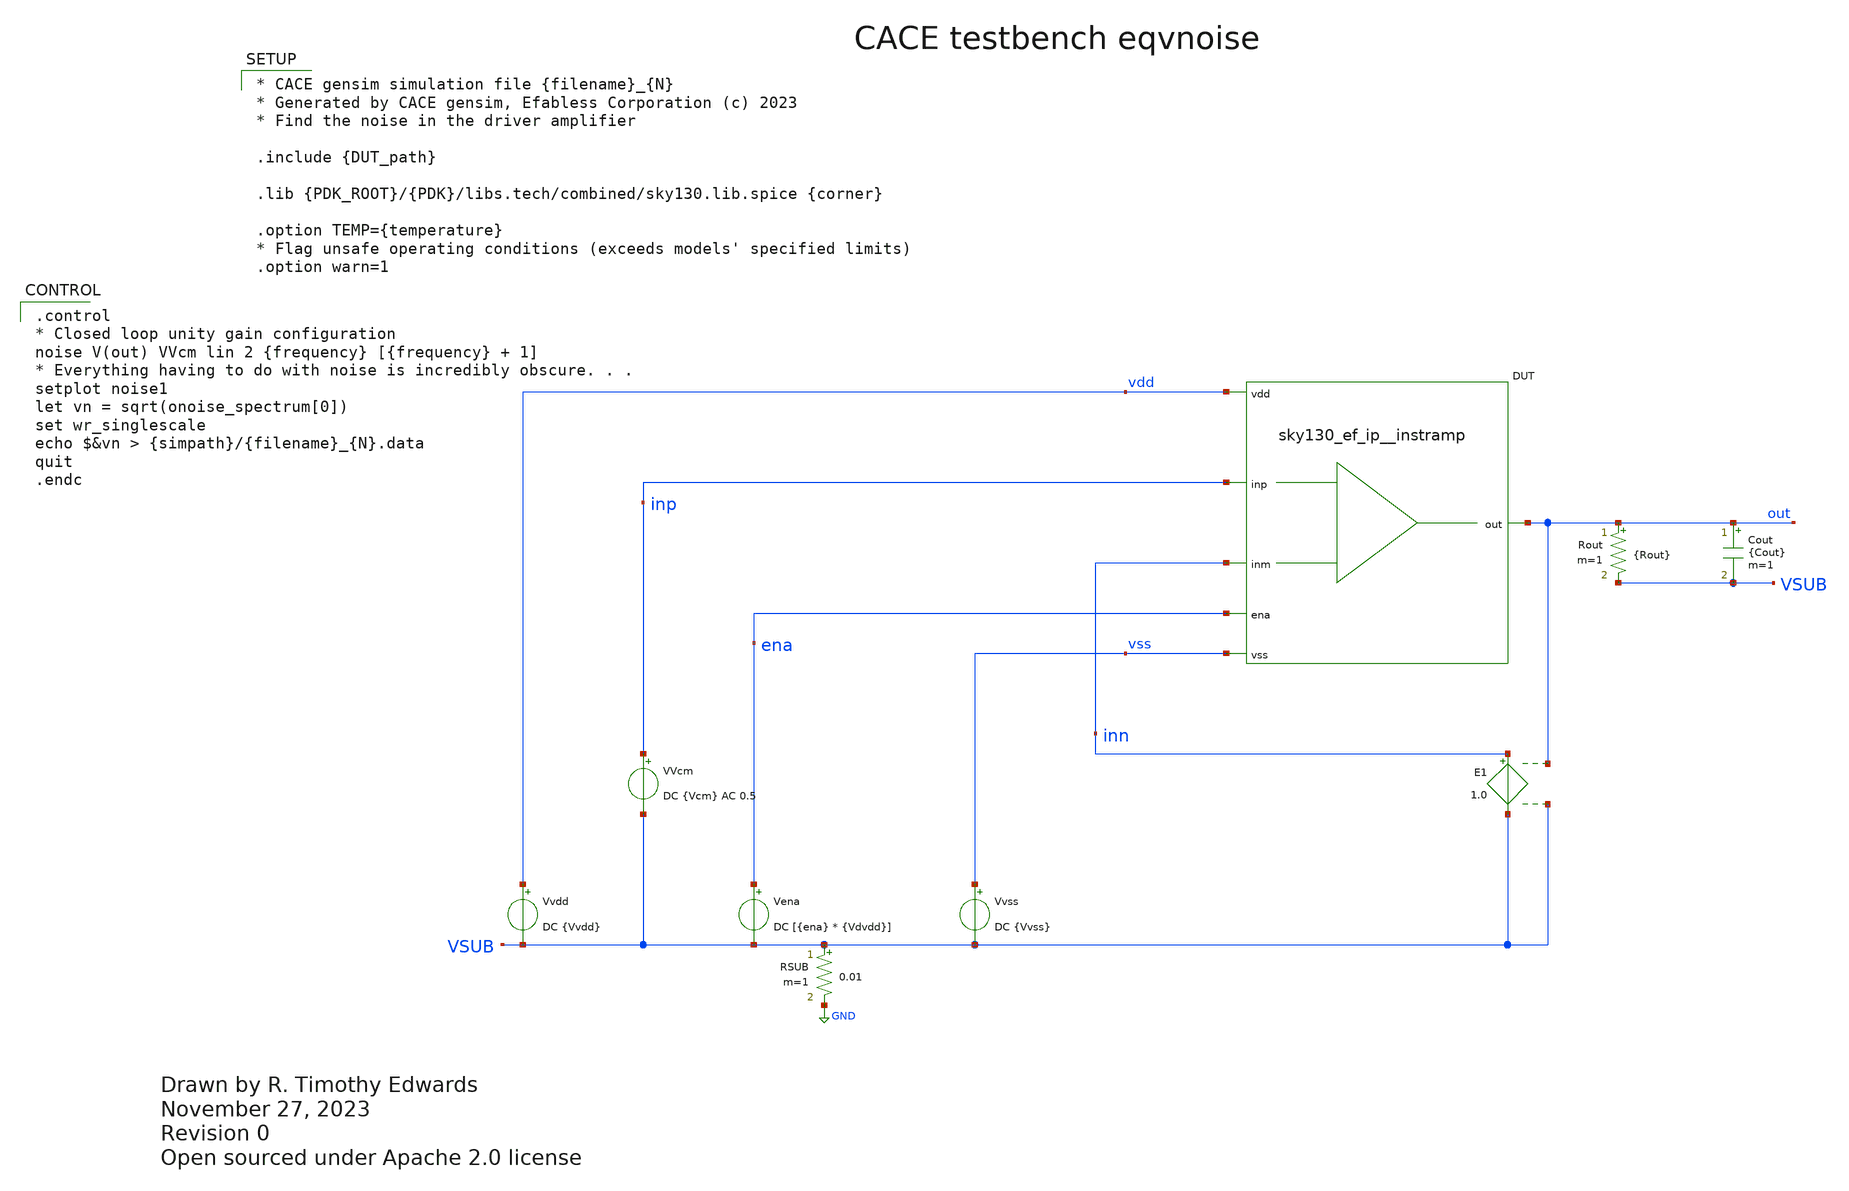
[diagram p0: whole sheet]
** sch_path: cace/eqvnoise.sch
* Open sourced under Apache 2.0 license
**.subckt eqvnoise
VVcm inp VSUB DC {Vcm} AC 0.5
Vena ena VSUB DC [{ena} * {Vdvdd}]
Vvss vss VSUB DC {Vvss}
Rout out VSUB {Rout} m=1
Cout out VSUB {Cout} m=1
Vvdd vdd VSUB DC {Vvdd}
RSUB VSUB GND 0.01 m=1
XDUT {PIN|vdd|vdd} {PIN|vss|vss} {PIN|inn|inm} {PIN|inp|inp} {PIN|out|out} {PIN|ena|ena} {DUT_name}
E1 inn VSUB out VSUB 1.0
**** begin user architecture code

.control
* Closed loop unity gain configuration
noise V(out) VVcm lin 2 {frequency} [{frequency} + 1]
* Everything having to do with noise is incredibly obscure. . .
setplot noise1
let vn = sqrt(onoise_spectrum[0])
set wr_singlescale
echo $&vn > {simpath}/{filename}_{N}.data
quit
.endc



* CACE gensim simulation file {filename}_{N}
* Generated by CACE gensim, Efabless Corporation (c) 2023
* Find the noise in the driver amplifier

.include {DUT_path}

.lib {PDK_ROOT}/{PDK}/libs.tech/combined/sky130.lib.spice {corner}

.option TEMP={temperature}
* Flag unsafe operating conditions (exceeds models' specified limits)
.option warn=1


**** end user architecture code
**.ends
.GLOBAL GND
.end
